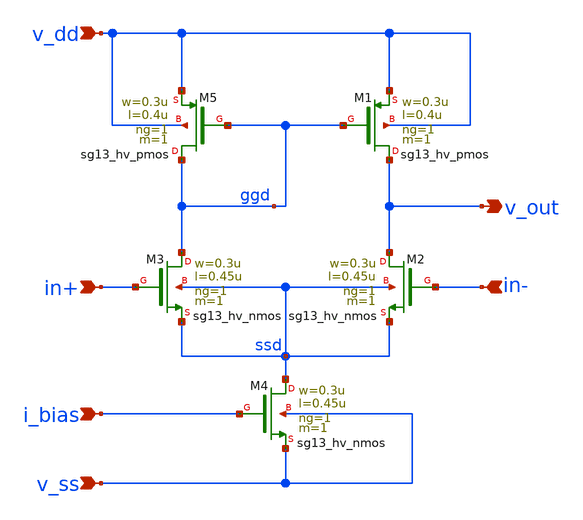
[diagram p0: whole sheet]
** sch_path: 3_Real_Cir/self_build_opamp.sch
**.subckt self_build_opamp in+ in- v_ss v_dd i_bias v_out
*.ipin in+
*.ipin in-
*.ipin v_ss
*.ipin v_dd
*.ipin i_bias
*.opin v_out
XM3 ggd in+ ssd ssd sg13_hv_nmos w=0.3u l=0.45u ng=1 m=1 mm_ok=1
XM2 v_out in- ssd ssd sg13_hv_nmos w=0.3u l=0.45u ng=1 m=1 mm_ok=1
XM4 ssd i_bias v_ss v_ss sg13_hv_nmos w=0.3u l=0.45u ng=1 m=1 mm_ok=1
XM5 ggd ggd v_dd v_dd sg13_hv_pmos w=0.3u l=0.4u ng=1 m=1 mm_ok=1
XM1 v_out ggd v_dd v_dd sg13_hv_pmos w=0.3u l=0.4u ng=1 m=1 mm_ok=1
**.ends
.end
